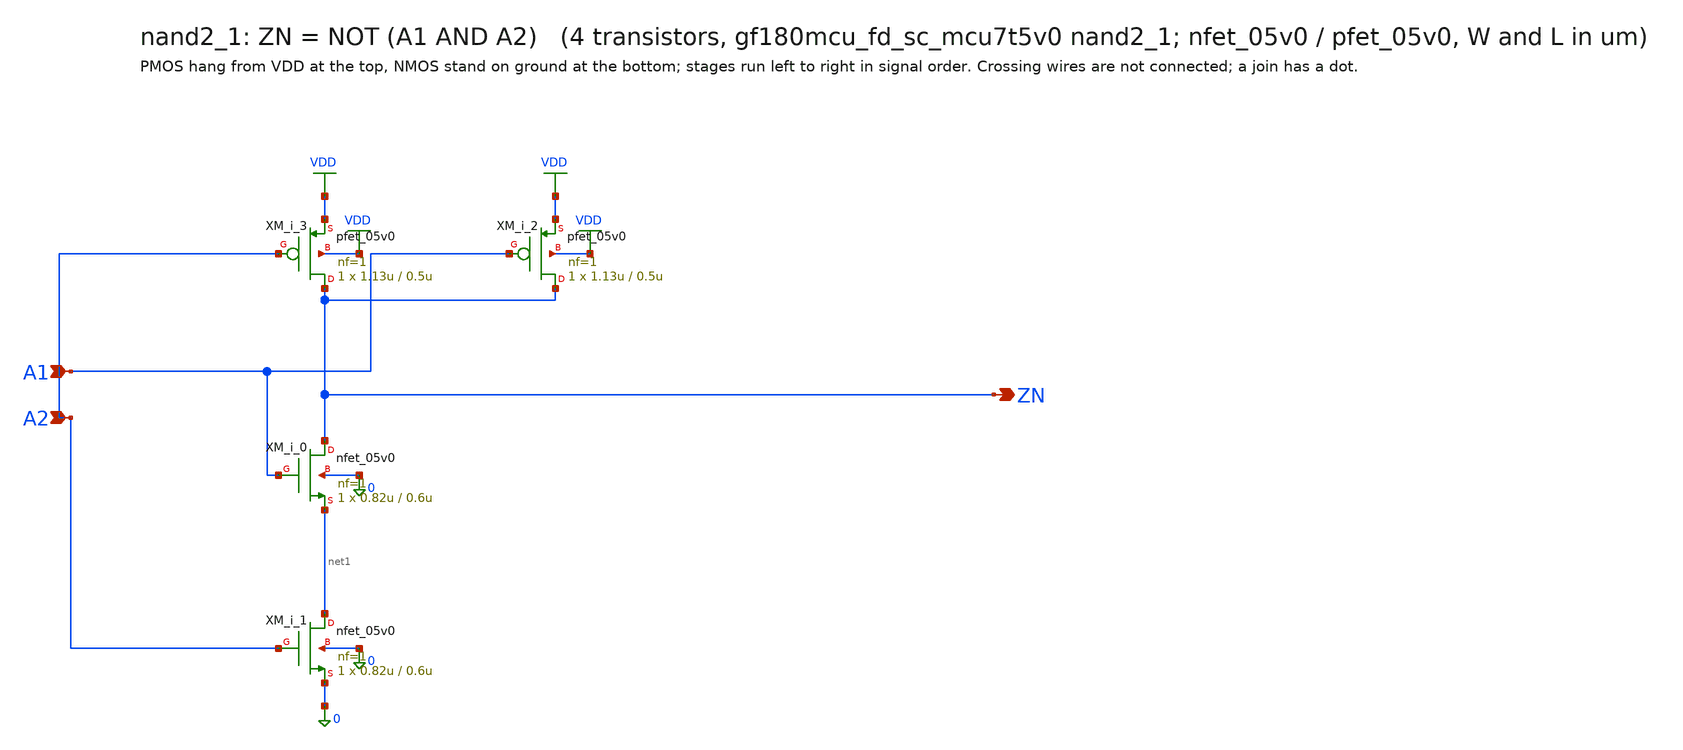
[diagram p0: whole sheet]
** sch_path: xschem/cells_tx/nand2_1.sch
**.subckt nand2_1 A1 A2 ZN
*.ipin A1
*.ipin A2
*.opin ZN
XM_i_1 net1 A2 0 0 nfet_05v0 L=0.6u W=0.82u nf=1 ad=4.1e-13 as=4.1e-13 pd=2.64e-06 ps=2.64e-06 nrd=0
+ nrs=0 sa=0 sb=0 sd=0 m=1
XM_i_0 ZN A1 net1 0 nfet_05v0 L=0.6u W=0.82u nf=1 ad=4.1e-13 as=4.1e-13 pd=2.64e-06 ps=2.64e-06
+ nrd=0 nrs=0 sa=0 sb=0 sd=0 m=1
XM_i_3 ZN A2 VDD VDD pfet_05v0 L=0.5u W=1.13u nf=1 ad=5.65e-13 as=5.65e-13 pd=3.26e-06 ps=3.26e-06
+ nrd=0 nrs=0 sa=0 sb=0 sd=0 m=1
XM_i_2 ZN A1 VDD VDD pfet_05v0 L=0.5u W=1.13u nf=1 ad=5.65e-13 as=5.65e-13 pd=3.26e-06 ps=3.26e-06
+ nrd=0 nrs=0 sa=0 sb=0 sd=0 m=1
**.ends
.GLOBAL VDD
.end
